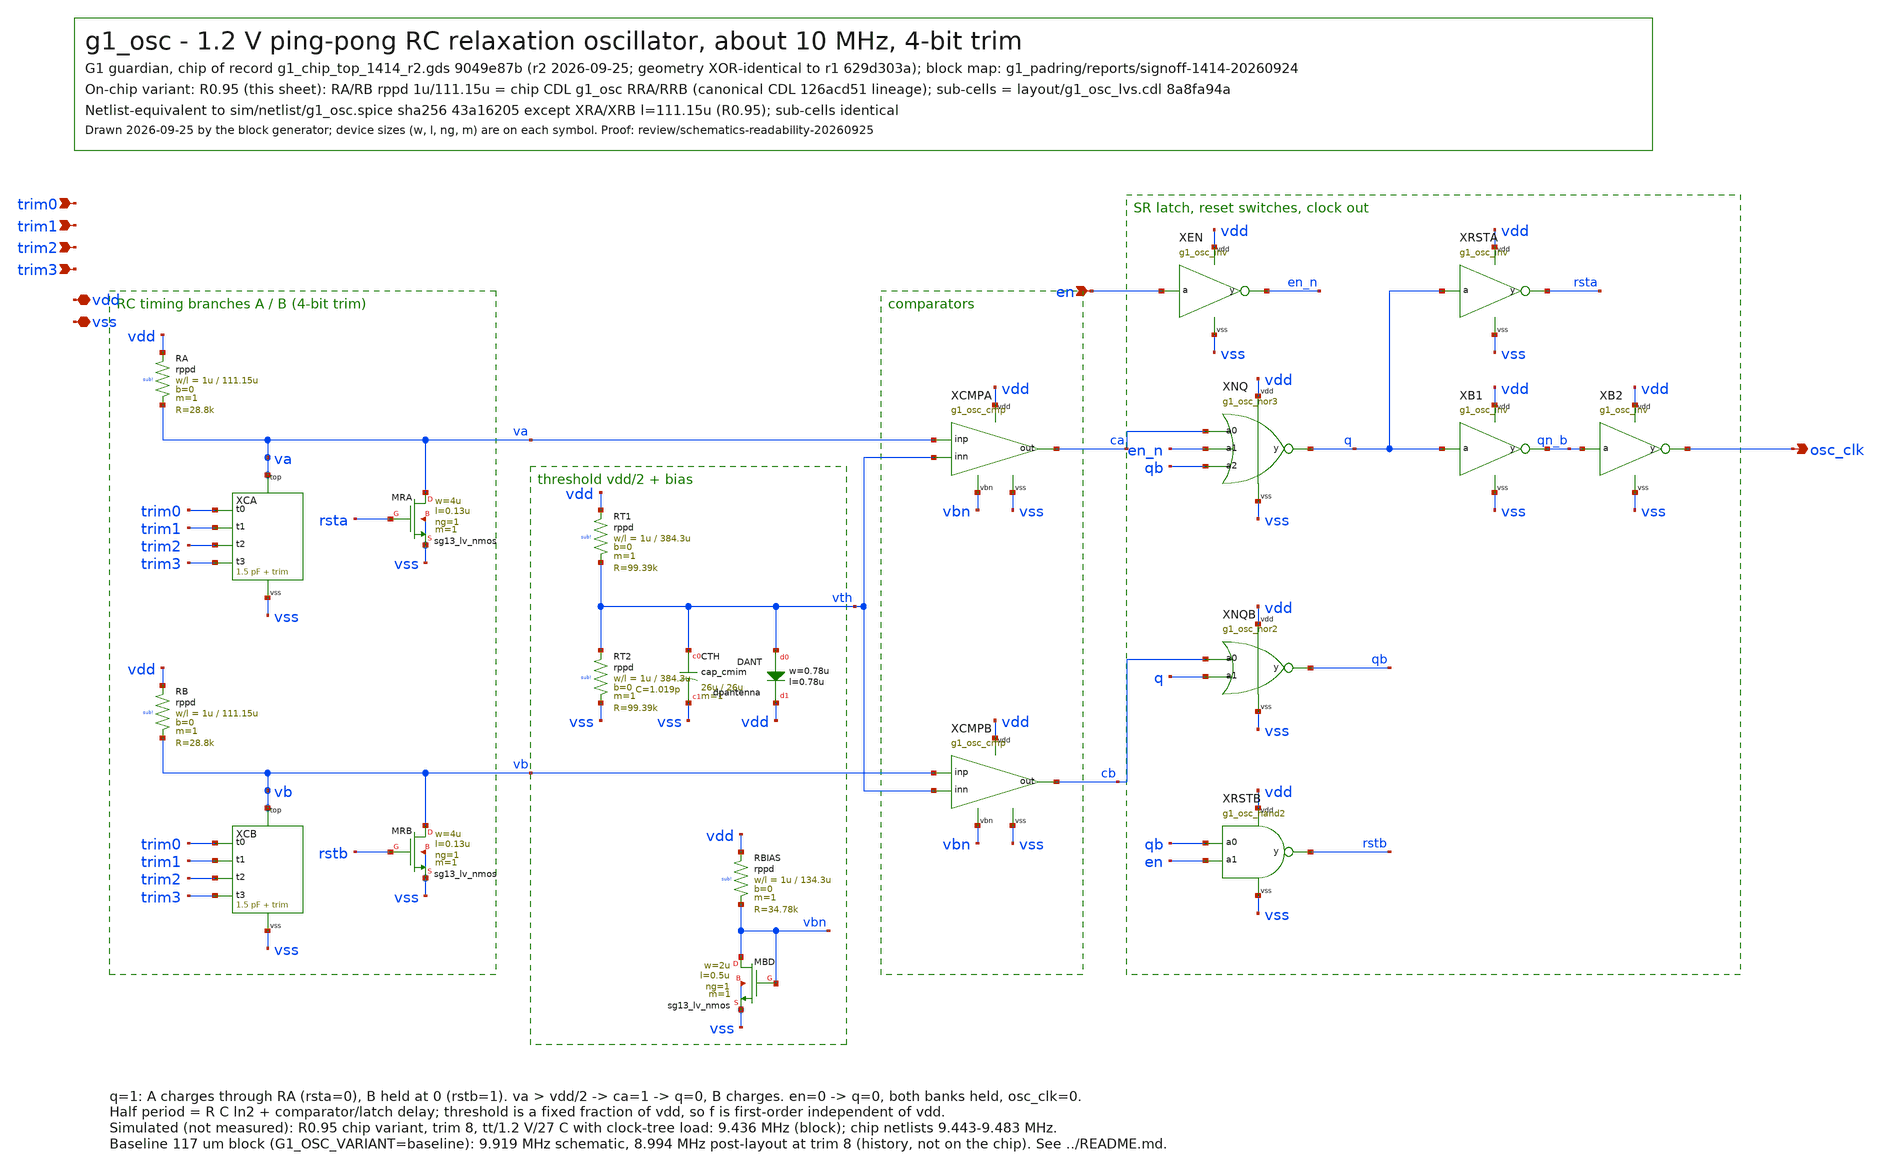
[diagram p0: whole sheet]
** sch_path: designs/g1-guardian/blocks/g1_osc/schematic/g1_osc.sch
**.subckt g1_osc en trim0 trim1 trim2 trim3 osc_clk vdd vss
*.ipin en
*.ipin trim0
*.ipin trim1
*.ipin trim2
*.ipin trim3
*.opin osc_clk
*.iopin vdd
*.iopin vss
XRA vdd va sub! rppd w=1u l=111.15u m=1 b=0 mm_ok=1
XRB vdd vb sub! rppd w=1u l=111.15u m=1 b=0 mm_ok=1
XCA trim0 trim1 trim2 trim3 va vss g1_osc_cbank
XCB trim0 trim1 trim2 trim3 vb vss g1_osc_cbank
XMRA va rsta vss vss sg13_lv_nmos w=4u l=0.13u ng=1 m=1 mm_ok=1
XMRB vb rstb vss vss sg13_lv_nmos w=4u l=0.13u ng=1 m=1 mm_ok=1
XRT1 vdd vth sub! rppd w=1u l=384.3u m=1 b=0 mm_ok=1
XRT2 vth vss sub! rppd w=1u l=384.3u m=1 b=0 mm_ok=1
XCTH vth vss cap_cmim w=26u l=26u m=1 mm_ok=1
XDANT vth vdd dpantenna l=0.78u w=0.78u
XRBIAS vdd vbn sub! rppd w=1u l=134.3u m=1 b=0 mm_ok=1
XMBD vbn vbn vss vss sg13_lv_nmos w=2u l=0.5u ng=1 m=1 mm_ok=1
XCMPA va vth vbn ca vdd vss g1_osc_cmp
XCMPB vb vth vbn cb vdd vss g1_osc_cmp
XEN en en_n vdd vss g1_osc_inv
XNQ ca en_n qb q vdd vss g1_osc_nor3
XNQB cb q qb vdd vss g1_osc_nor2
XRSTB qb en rstb vdd vss g1_osc_nand2
XRSTA q rsta vdd vss g1_osc_inv
XB1 q qn_b vdd vss g1_osc_inv
XB2 qn_b osc_clk vdd vss g1_osc_inv
**.ends

* expanding   symbol:  g1_osc_cbank.sym # of pins=6
** sym_path: designs/g1-guardian/blocks/g1_osc/schematic/g1_osc_cbank.sym
** sch_path: designs/g1-guardian/blocks/g1_osc/schematic/g1_osc_cbank.sch
.subckt g1_osc_cbank t0 t1 t2 t3 top vss
*.ipin t0
*.ipin t1
*.ipin t2
*.ipin t3
*.iopin top
*.iopin vss
XCF top vss cap_cmim w=31.65u l=31.65u m=1 mm_ok=1
XCT0 top b0 cap_cmim w=8.16u l=8.16u m=1 mm_ok=1
XMS0 b0 t0 vss vss sg13_lv_nmos w=4u l=0.13u ng=1 m=1 mm_ok=1
XCT1 top b1 cap_cmim w=11.55u l=11.55u m=1 mm_ok=1
XMS1 b1 t1 vss vss sg13_lv_nmos w=4u l=0.13u ng=1 m=1 mm_ok=1
XCT2 top b2 cap_cmim w=16.33u l=16.33u m=1 mm_ok=1
XMS2 b2 t2 vss vss sg13_lv_nmos w=4u l=0.13u ng=1 m=1 mm_ok=1
XCT3 top b3 cap_cmim w=23.09u l=23.09u m=1 mm_ok=1
XMS3 b3 t3 vss vss sg13_lv_nmos w=4u l=0.13u ng=1 m=1 mm_ok=1
.ends


* expanding   symbol:  g1_osc_cmp.sym # of pins=6
** sym_path: designs/g1-guardian/blocks/g1_osc/schematic/g1_osc_cmp.sym
** sch_path: designs/g1-guardian/blocks/g1_osc/schematic/g1_osc_cmp.sch
.subckt g1_osc_cmp inp inn vbn out vdd vss
*.ipin inp
*.ipin inn
*.ipin vbn
*.opin out
*.iopin vdd
*.iopin vss
XMT tail vbn vss vss sg13_lv_nmos w=2u l=0.5u ng=1 m=1 mm_ok=1
XM1 d1 inp tail vss sg13_lv_nmos w=4u l=0.3u ng=1 m=1 mm_ok=1
XM2 o1 inn tail vss sg13_lv_nmos w=4u l=0.3u ng=1 m=1 mm_ok=1
XM3 d1 d1 vdd vdd sg13_lv_pmos w=2u l=0.3u ng=1 m=1 mm_ok=1
XM4 o1 d1 vdd vdd sg13_lv_pmos w=2u l=0.3u ng=1 m=1 mm_ok=1
XI1 o1 o2 vdd vss g1_osc_inv
XI2 o2 out vdd vss g1_osc_inv
.ends


* expanding   symbol:  g1_osc_inv.sym # of pins=4
** sym_path: designs/g1-guardian/blocks/g1_osc/schematic/g1_osc_inv.sym
** sch_path: designs/g1-guardian/blocks/g1_osc/schematic/g1_osc_inv.sch
.subckt g1_osc_inv a y vdd vss
*.ipin a
*.opin y
*.iopin vdd
*.iopin vss
XMP y a vdd vdd sg13_lv_pmos w=1u l=0.13u ng=1 m=1 mm_ok=1
XMN y a vss vss sg13_lv_nmos w=0.5u l=0.13u ng=1 m=1 mm_ok=1
.ends


* expanding   symbol:  g1_osc_nor3.sym # of pins=6
** sym_path: designs/g1-guardian/blocks/g1_osc/schematic/g1_osc_nor3.sym
** sch_path: designs/g1-guardian/blocks/g1_osc/schematic/g1_osc_nor3.sch
.subckt g1_osc_nor3 a0 a1 a2 y vdd vss
*.ipin a0
*.ipin a1
*.ipin a2
*.opin y
*.iopin vdd
*.iopin vss
XMP0 p0 a0 vdd vdd sg13_lv_pmos w=3u l=0.13u ng=1 m=1 mm_ok=1
XMP1 p1 a1 p0 vdd sg13_lv_pmos w=3u l=0.13u ng=1 m=1 mm_ok=1
XMP2 y a2 p1 vdd sg13_lv_pmos w=3u l=0.13u ng=1 m=1 mm_ok=1
XMN0 y a0 vss vss sg13_lv_nmos w=0.5u l=0.13u ng=1 m=1 mm_ok=1
XMN1 y a1 vss vss sg13_lv_nmos w=0.5u l=0.13u ng=1 m=1 mm_ok=1
XMN2 y a2 vss vss sg13_lv_nmos w=0.5u l=0.13u ng=1 m=1 mm_ok=1
.ends


* expanding   symbol:  g1_osc_nor2.sym # of pins=5
** sym_path: designs/g1-guardian/blocks/g1_osc/schematic/g1_osc_nor2.sym
** sch_path: designs/g1-guardian/blocks/g1_osc/schematic/g1_osc_nor2.sch
.subckt g1_osc_nor2 a0 a1 y vdd vss
*.ipin a0
*.ipin a1
*.opin y
*.iopin vdd
*.iopin vss
XMP0 p0 a0 vdd vdd sg13_lv_pmos w=2u l=0.13u ng=1 m=1 mm_ok=1
XMP1 y a1 p0 vdd sg13_lv_pmos w=2u l=0.13u ng=1 m=1 mm_ok=1
XMN0 y a0 vss vss sg13_lv_nmos w=0.5u l=0.13u ng=1 m=1 mm_ok=1
XMN1 y a1 vss vss sg13_lv_nmos w=0.5u l=0.13u ng=1 m=1 mm_ok=1
.ends


* expanding   symbol:  g1_osc_nand2.sym # of pins=5
** sym_path: designs/g1-guardian/blocks/g1_osc/schematic/g1_osc_nand2.sym
** sch_path: designs/g1-guardian/blocks/g1_osc/schematic/g1_osc_nand2.sch
.subckt g1_osc_nand2 a0 a1 y vdd vss
*.ipin a0
*.ipin a1
*.opin y
*.iopin vdd
*.iopin vss
XMP0 y a0 vdd vdd sg13_lv_pmos w=1u l=0.13u ng=1 m=1 mm_ok=1
XMP1 y a1 vdd vdd sg13_lv_pmos w=1u l=0.13u ng=1 m=1 mm_ok=1
XMN0 y a0 n0 vss sg13_lv_nmos w=1u l=0.13u ng=1 m=1 mm_ok=1
XMN1 n0 a1 vss vss sg13_lv_nmos w=1u l=0.13u ng=1 m=1 mm_ok=1
.ends

.end
